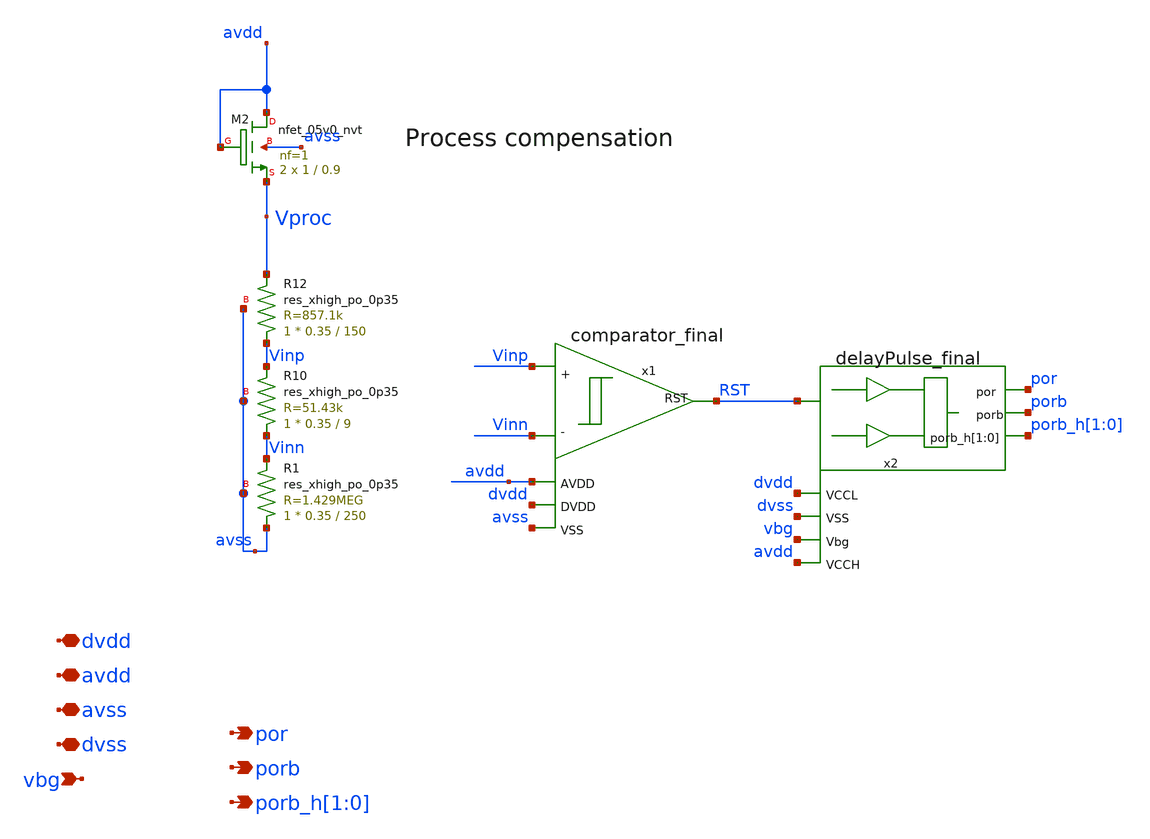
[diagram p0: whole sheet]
** sch_path: xschem/sky130_sw_ip__bgrref_por.sch
**.subckt sky130_sw_ip__bgrref_por avdd por avss dvdd porb vbg porb_h[1],porb_h[0] dvss
*.iopin avdd
*.opin por
*.iopin avss
*.iopin dvdd
*.opin porb
*.ipin vbg
*.opin porb_h[1],porb_h[0]
*.iopin dvss
x1 Vinn Vinp RST avss avdd dvdd comparator_final
XR1 avss Vinn avss sky130_fd_pr__res_xhigh_po_0p35 L=250 mult=1 m=1
XR10 Vinn Vinp avss sky130_fd_pr__res_xhigh_po_0p35 L=9 mult=1 m=1
XR12 Vinp Vproc avss sky130_fd_pr__res_xhigh_po_0p35 L=150 mult=1 m=1
x2 RST por dvdd dvss vbg avdd porb porb_h[1] porb_h[0] delayPulse_final
XM2 avdd avdd Vproc avss sky130_fd_pr__nfet_05v0_nvt L=0.9 W=1 nf=1 ad='int((nf+1)/2) * W/nf * 0.29'
+ as='int((nf+2)/2) * W/nf * 0.29' pd='2*int((nf+1)/2) * (W/nf + 0.29)' ps='2*int((nf+2)/2) * (W/nf + 0.29)'
+ nrd='0.29 / W' nrs='0.29 / W' sa=0 sb=0 sd=0 mult=2 m=2
**.ends
.end
